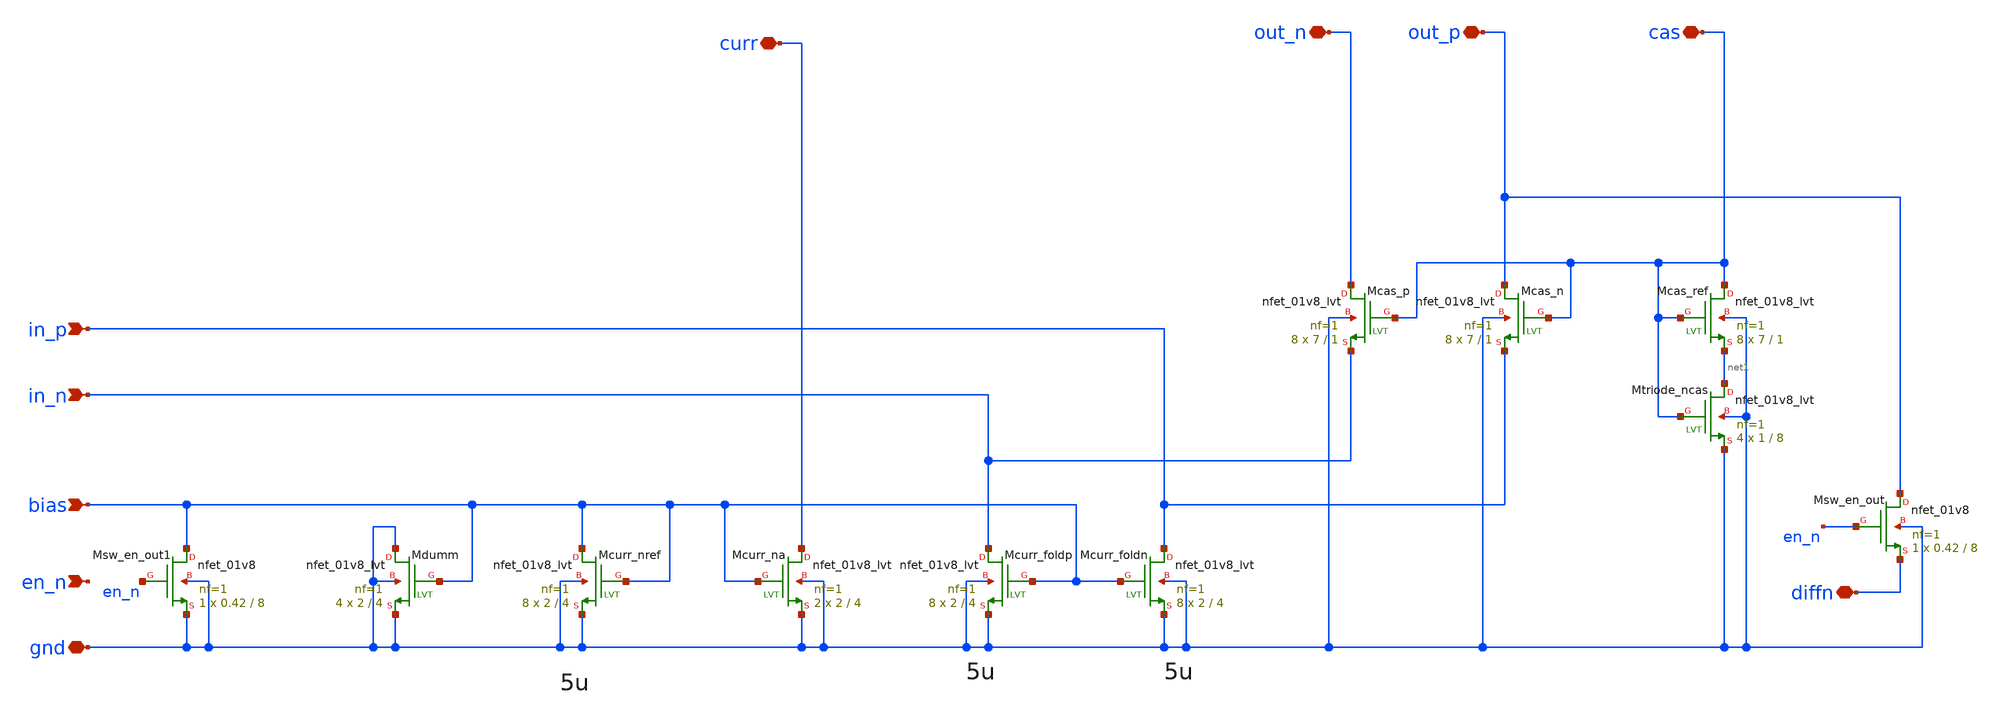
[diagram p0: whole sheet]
** sch_path: design/bandgap_opamp_nmos/bandgap_opamp_nmos.sch
**.subckt bandgap_opamp_nmos in_p in_n bias out_p gnd en_n out_n cas curr diffn
*.ipin in_p
*.ipin in_n
*.ipin bias
*.iopin out_p
*.iopin gnd
*.ipin en_n
*.iopin out_n
*.iopin cas
*.iopin curr
*.iopin diffn
XMcurr_nref bias bias gnd gnd sky130_fd_pr__nfet_01v8_lvt L=4 W=2 nf=1 ad='W * 0.29' as='W * 0.29' pd='2 * (W + 0.29)'
+ ps='2 * (W + 0.29)' nrd='0.29 / W' nrs='0.29 / W' sa=0 sb=0 sd=0 mult=8 m=8
XMcurr_na curr bias gnd gnd sky130_fd_pr__nfet_01v8_lvt L=4 W=2 nf=1 ad='W * 0.29' as='W * 0.29' pd='2 * (W + 0.29)'
+ ps='2 * (W + 0.29)' nrd='0.29 / W' nrs='0.29 / W' sa=0 sb=0 sd=0 mult=2 m=2
XMtriode_ncas net1 cas gnd gnd sky130_fd_pr__nfet_01v8_lvt L=8 W=1 nf=1 ad='W * 0.29' as='W * 0.29' pd='2 * (W + 0.29)'
+ ps='2 * (W + 0.29)' nrd='0.29 / W' nrs='0.29 / W' sa=0 sb=0 sd=0 mult=4 m=4
XMcas_ref cas cas net1 gnd sky130_fd_pr__nfet_01v8_lvt L=1 W=7 nf=1 ad='W * 0.29' as='W * 0.29' pd='2 * (W + 0.29)'
+ ps='2 * (W + 0.29)' nrd='0.29 / W' nrs='0.29 / W' sa=0 sb=0 sd=0 mult=8 m=8
XMcas_n out_p cas in_p gnd sky130_fd_pr__nfet_01v8_lvt L=1 W=7 nf=1 ad='W * 0.29' as='W * 0.29' pd='2 * (W + 0.29)'
+ ps='2 * (W + 0.29)' nrd='0.29 / W' nrs='0.29 / W' sa=0 sb=0 sd=0 mult=8 m=8
XMcas_p out_n cas in_n gnd sky130_fd_pr__nfet_01v8_lvt L=1 W=7 nf=1 ad='W * 0.29' as='W * 0.29' pd='2 * (W + 0.29)'
+ ps='2 * (W + 0.29)' nrd='0.29 / W' nrs='0.29 / W' sa=0 sb=0 sd=0 mult=8 m=8
XMcurr_foldn in_p bias gnd gnd sky130_fd_pr__nfet_01v8_lvt L=4 W=2 nf=1 ad='W * 0.29' as='W * 0.29' pd='2 * (W + 0.29)'
+ ps='2 * (W + 0.29)' nrd='0.29 / W' nrs='0.29 / W' sa=0 sb=0 sd=0 mult=8 m=8
XMcurr_foldp in_n bias gnd gnd sky130_fd_pr__nfet_01v8_lvt L=4 W=2 nf=1 ad='W * 0.29' as='W * 0.29' pd='2 * (W + 0.29)'
+ ps='2 * (W + 0.29)' nrd='0.29 / W' nrs='0.29 / W' sa=0 sb=0 sd=0 mult=8 m=8
XMsw_en_out out_p en_n diffn gnd sky130_fd_pr__nfet_01v8 L=8 W=0.42 nf=1 ad='W * 0.29' as='W * 0.29'
+ pd='2 * (W + 0.29)' ps='2 * (W + 0.29)' nrd='0.29 / W' nrs='0.29 / W' sa=0 sb=0 sd=0 mult=1 m=1
XMsw_en_out1 bias en_n gnd gnd sky130_fd_pr__nfet_01v8 L=8 W=0.42 nf=1 ad='W * 0.29' as='W * 0.29' pd='2 * (W + 0.29)'
+ ps='2 * (W + 0.29)' nrd='0.29 / W' nrs='0.29 / W' sa=0 sb=0 sd=0 mult=1 m=1
XMdumm gnd bias gnd gnd sky130_fd_pr__nfet_01v8_lvt L=4 W=2 nf=1 ad='W * 0.29' as='W * 0.29' pd='2 * (W + 0.29)'
+ ps='2 * (W + 0.29)' nrd='0.29 / W' nrs='0.29 / W' sa=0 sb=0 sd=0 mult=4 m=4
**.ends
.end
